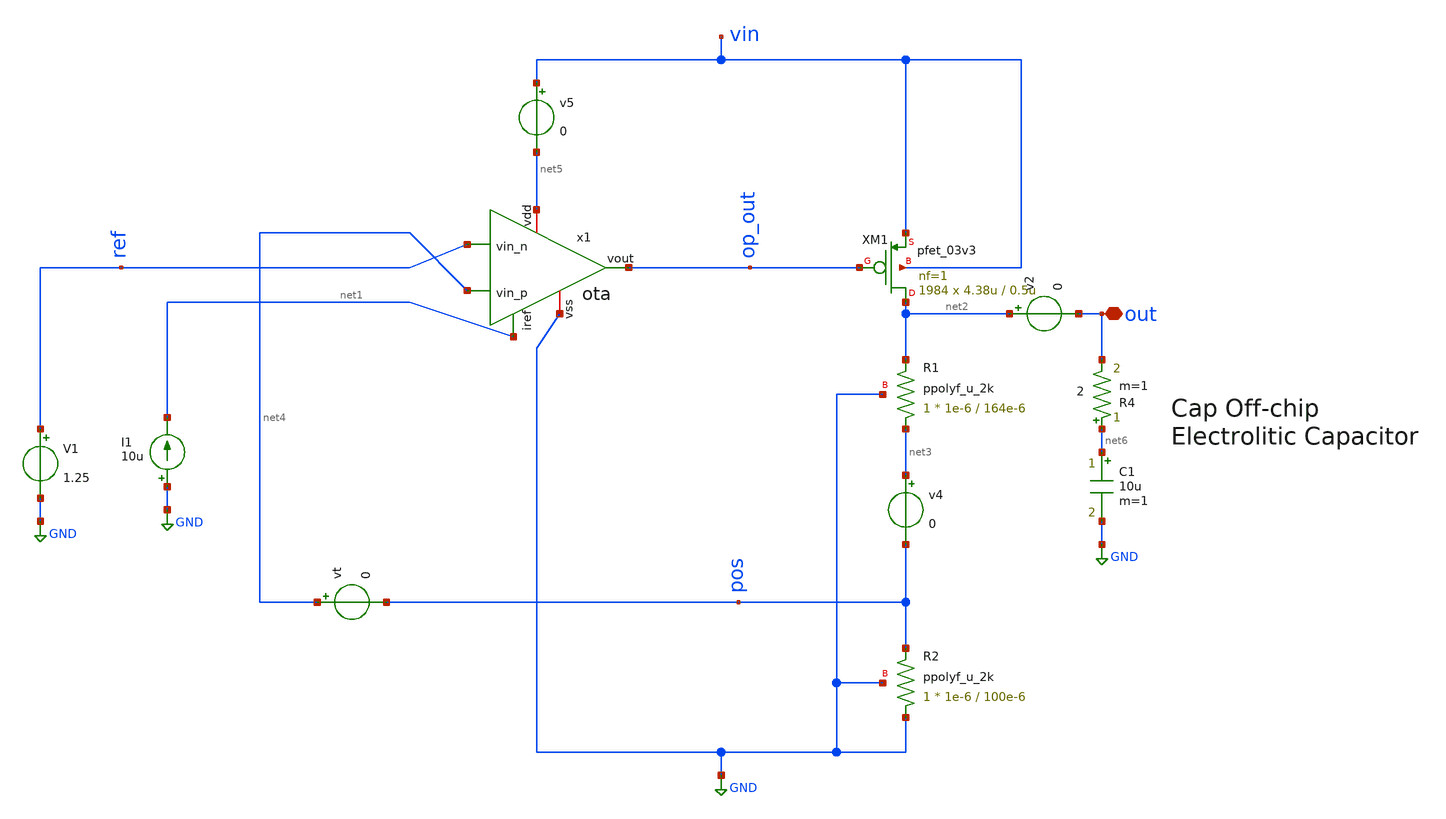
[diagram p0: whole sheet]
** sch_path: LDO/xschem/ldo/test/psrr.sch

.include $env(PDK_ROOT)/$env(PDK)/libs.tech/ngspice/design.ngspice
.lib $env(PDK_ROOT)/$env(PDK)/libs.tech/ngspice/sm141064.ngspice typical
.lib $env(PDK_ROOT)/$env(PDK)/libs.tech/ngspice/sm141064.ngspice res_typical

.lib $env(PDK_ROOT)/$env(PDK)/libs.tech/ngspice/sm141064.ngspice cap_mim
.lib $env(PDK_ROOT)/$env(PDK)/libs.tech/ngspice/sm141064.ngspice mimcap_typical


**.subckt psrr out
*.iopin out
I1 GND net1 10u
V1 ref GND 1.25
XM1 net2 op_out vin vin pfet_03v3 L=0.5u W=4.38u nf=1 ad='int((nf+1)/2) * W/nf * 0.18u' as='int((nf+2)/2) * W/nf * 0.18u'
+ pd='2*int((nf+1)/2) * (W/nf + 0.18u)' ps='2*int((nf+2)/2) * (W/nf + 0.18u)' nrd='0.18u / W' nrs='0.18u / W'
+ sa=0 sb=0 sd=0 m=1984
XR1 net3 net2 GND ppolyf_u_2k r_width=1e-6 r_length=164e-6 m=1
XR2 GND pos GND ppolyf_u_2k r_width=1e-6 r_length=100e-6 m=1
v4 net3 pos 0
vt net4 pos 0
v2 net2 out 0
v5 vin net5 0
x1 net5 net1 ref net4 op_out GND ota
C1 net6 GND 10u m=1
R4 net6 out 2 m=1
**** begin user architecture code


.param R=33
R10 out 0 {R}
IL out 0 PWL(0 0.1m 10u 0.1m 20u 10m 30u 10m)

.param iref = 10u
.param vdd  = 5
.param vss  = 0.0
.param vcm  = 1.25
.param vac  = 60m
.param w857 = 5u
.param l857 = 1u
.param m857 = 1
.param wpar = 10u
.param lpar = 1u
.param mpar = 1
.param w34  = 10u
.param l34  = 1u
.param m34  = 1
.param w6   = 100u
.param l6   = 1u
.param m6   = 1

.param m5   = 1
.param m7   = 5


Vs vin 0 5

.nodeset v(out)=0
.nodeset v(x1.pos)=0

*PSRR_Analysis
.control
reset
alter Vs AC =1
alter Vt AC=0
ac dec 100 1 1G
plot vdb(out)
let phase_val = 180/PI*cph(out)
plot phase_val
*plot (180/pi)*vp(out)
*let gm0=@m.xm0.m0[gm]
*let Zout=(1.5)/(gm0*v(op_out))
*let Zout2=v(out)/gm0
*plot vdb(Zout2)
*wrdata /foss/designs/LDO_Design/data/data_PSRR.dat vdb(out)
meas ac gain_1kh FIND vdb(out) WHEN frequency=1000
.endc


**** end user architecture code
**.ends
.GLOBAL GND
.end
